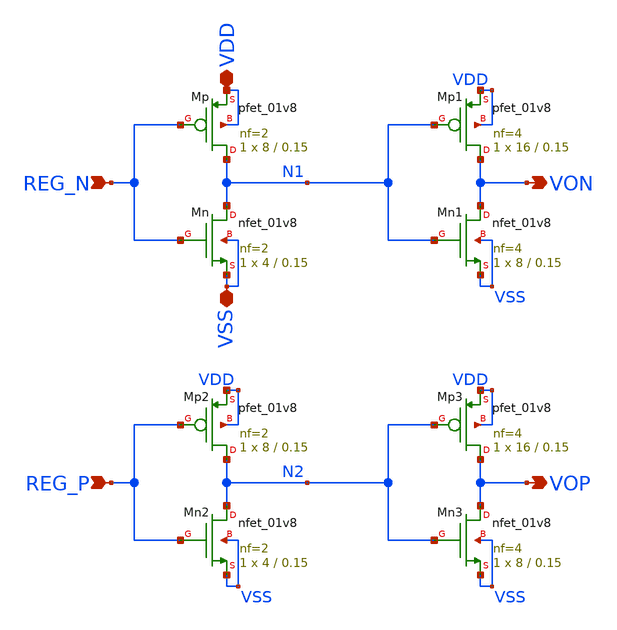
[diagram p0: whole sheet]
** sch_path: strongarm_buffer.sch
**.subckt strongarm_buffer REG_N REG_P VON VOP VDD VSS
*.ipin REG_N
*.ipin REG_P
*.opin VON
*.opin VOP
*.iopin VDD
*.iopin VSS
XMp N1 REG_N VDD VDD sky130_fd_pr__pfet_01v8 L=0.15 W=8 nf=2 ad='int((2 + 1)/2) * 8 / 2 * 0.29' as='int((2 + 2)/2) * 8 / 2 * 0.29'
+ pd='2*int((2 + 1)/2) * (8 / 2 + 0.29)' ps='2*int((2 + 2)/2) * (8 / 2 + 0.29)' nrd='0.29 / 8 ' nrs='0.29 / 8 '
+ sa=0 sb=0 sd=0 mult=1 m=1
XMn N1 REG_N VSS VSS sky130_fd_pr__nfet_01v8 L=0.15 W=4 nf=2 ad='int((2 + 1)/2) * 4 / 2 * 0.29' as='int((2 + 2)/2) * 4 / 2 * 0.29'
+ pd='2*int((2 + 1)/2) * (4 / 2 + 0.29)' ps='2*int((2 + 2)/2) * (4 / 2 + 0.29)' nrd='0.29 / 4 ' nrs='0.29 / 4 '
+ sa=0 sb=0 sd=0 mult=1 m=1
XMp1 VON N1 VDD VDD sky130_fd_pr__pfet_01v8 L=0.15 W=16 nf=4 ad='int((4 + 1)/2) * 16 / 4 * 0.29' as='int((4 + 2)/2) * 16 / 4 * 0.29'
+ pd='2*int((4 + 1)/2) * (16 / 4 + 0.29)' ps='2*int((4 + 2)/2) * (16 / 4 + 0.29)' nrd='0.29 / 16 ' nrs='0.29 / 16 '
+ sa=0 sb=0 sd=0 mult=1 m=1
XMn1 VON N1 VSS VSS sky130_fd_pr__nfet_01v8 L=0.15 W=8 nf=4 ad='int((4 + 1)/2) * 8 / 4 * 0.29' as='int((4 + 2)/2) * 8 / 4 * 0.29'
+ pd='2*int((4 + 1)/2) * (8 / 4 + 0.29)' ps='2*int((4 + 2)/2) * (8 / 4 + 0.29)' nrd='0.29 / 8 ' nrs='0.29 / 8 '
+ sa=0 sb=0 sd=0 mult=1 m=1
XMp2 N2 REG_P VDD VDD sky130_fd_pr__pfet_01v8 L=0.15 W=8 nf=2 ad='int((2 + 1)/2) * 8 / 2 * 0.29' as='int((2 + 2)/2) * 8 / 2 * 0.29'
+ pd='2*int((2 + 1)/2) * (8 / 2 + 0.29)' ps='2*int((2 + 2)/2) * (8 / 2 + 0.29)' nrd='0.29 / 8 ' nrs='0.29 / 8 '
+ sa=0 sb=0 sd=0 mult=1 m=1
XMn2 N2 REG_P VSS VSS sky130_fd_pr__nfet_01v8 L=0.15 W=4 nf=2 ad='int((2 + 1)/2) * 4 / 2 * 0.29' as='int((2 + 2)/2) * 4 / 2 * 0.29'
+ pd='2*int((2 + 1)/2) * (4 / 2 + 0.29)' ps='2*int((2 + 2)/2) * (4 / 2 + 0.29)' nrd='0.29 / 4 ' nrs='0.29 / 4 '
+ sa=0 sb=0 sd=0 mult=1 m=1
XMp3 VOP N2 VDD VDD sky130_fd_pr__pfet_01v8 L=0.15 W=16 nf=4 ad='int((4 + 1)/2) * 16 / 4 * 0.29' as='int((4 + 2)/2) * 16 / 4 * 0.29'
+ pd='2*int((4 + 1)/2) * (16 / 4 + 0.29)' ps='2*int((4 + 2)/2) * (16 / 4 + 0.29)' nrd='0.29 / 16 ' nrs='0.29 / 16 '
+ sa=0 sb=0 sd=0 mult=1 m=1
XMn3 VOP N2 VSS VSS sky130_fd_pr__nfet_01v8 L=0.15 W=8 nf=4 ad='int((4 + 1)/2) * 8 / 4 * 0.29' as='int((4 + 2)/2) * 8 / 4 * 0.29'
+ pd='2*int((4 + 1)/2) * (8 / 4 + 0.29)' ps='2*int((4 + 2)/2) * (8 / 4 + 0.29)' nrd='0.29 / 8 ' nrs='0.29 / 8 '
+ sa=0 sb=0 sd=0 mult=1 m=1
**.ends
.end
